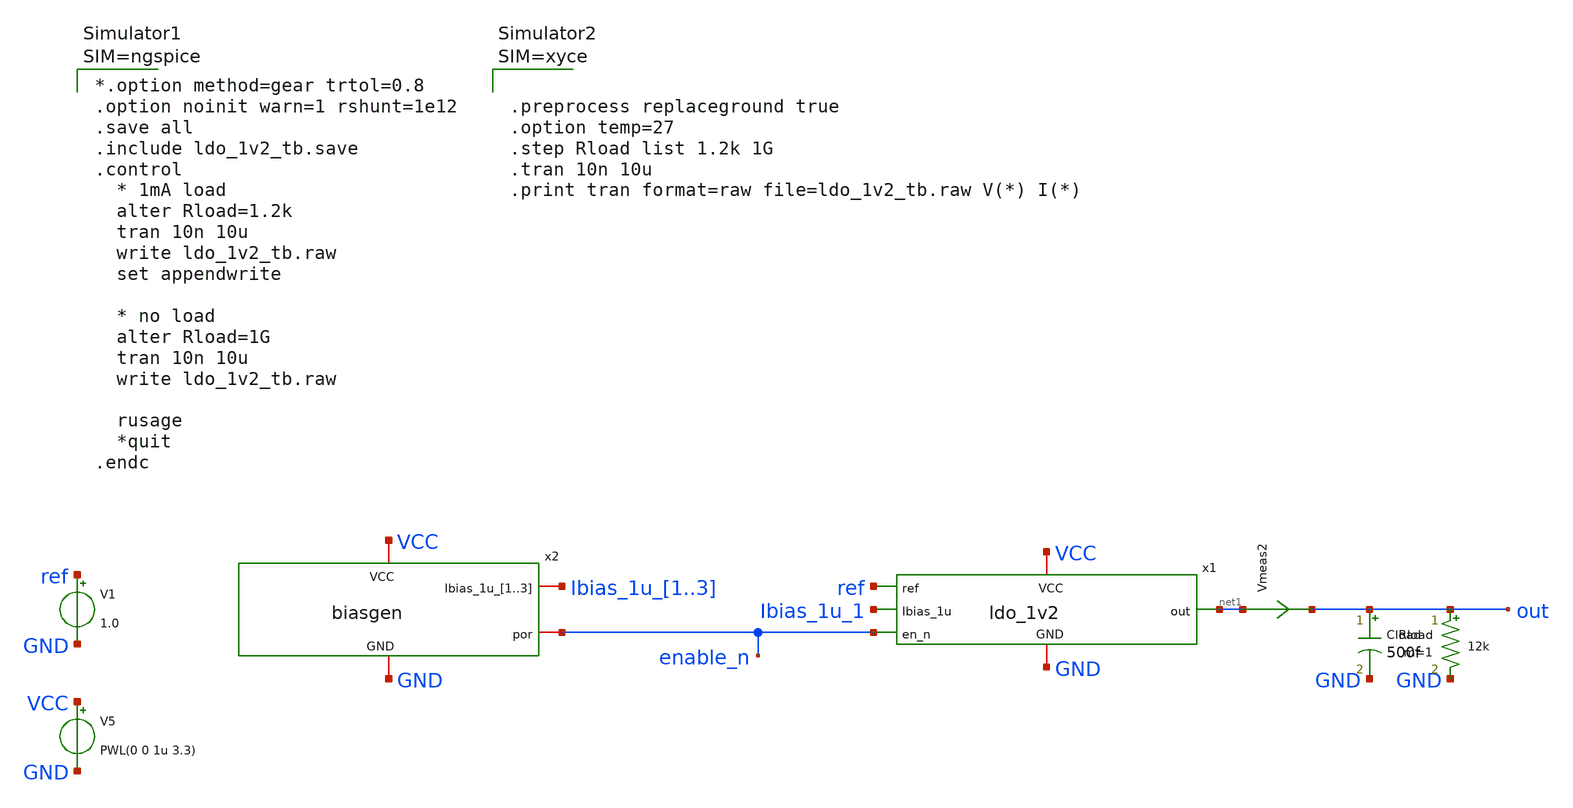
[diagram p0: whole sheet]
** sch_path: FLDO/design_data/xschem/ldo_1v2_tb.sch
**.subckt ldo_1v2_tb
x1 VCC GND ref Ibias_1u_1 net1 enable_n ldo_1v2
x2 VCC GND Ibias_1u_1 Ibias_1u_2 Ibias_1u_3 enable_n biasgen
V5 VCC GND PWL(0 0 1u 3.3)
V1 ref GND 1.0
Cload out GND 500f m=1
Rload out GND 12k m=1
Vmeas2 net1 out 0
.save i(vmeas2)
**** begin user architecture code









** IHP models
.lib cornerMOSlv.lib mos_tt
.lib cornerMOShv.lib mos_tt
.lib cornerHBT.lib hbt_typ
.lib cornerRES.lib res_typ
.lib cornerCAP.lib cap_typ

.include sg13g2_stdcell.spice






*.option method=gear trtol=0.8
.option noinit warn=1 rshunt=1e12
.save all
.include ldo_1v2_tb.save
.control
  * 1mA load
  alter Rload=1.2k
  tran 10n 10u
  write ldo_1v2_tb.raw
  set appendwrite

  * no load
  alter Rload=1G
  tran 10n 10u
  write ldo_1v2_tb.raw

  rusage
  *quit
.endc



**** end user architecture code
**.ends

* expanding   symbol:  ldo_1v2.sym # of pins=6
** sym_path: FLDO/design_data/xschem/ldo_1v2.sym
** sch_path: FLDO/design_data/xschem/ldo_1v2.sch
.subckt ldo_1v2 VCC GND ref Ibias_1u out en_n
*.iopin VCC
*.iopin GND
*.ipin ref
*.ipin Ibias_1u
*.opin out
*.ipin en_n
XM4 out vg net1 net1 sg13_hv_pmos w=50u l=0.4u ng=10 m=1 mm_ok=1
Vmeas VCC net1 0
.save i(vmeas)
XC1 out vg cap_cmim w=10.0e-6 l=10.0e-6 m=1
XM2 Ibias_1u en_n GND GND sg13_hv_nmos w=0.3u l=0.45u ng=1 m=1 mm_ok=1
XM3 vg en VCC VCC sg13_hv_pmos w=0.3u l=0.4u ng=1 m=1 mm_ok=1
XM1 en en_n GND GND sg13_hv_nmos w=0.3u l=0.45u ng=1 m=1 mm_ok=1
XM11 en en_n VCC VCC sg13_hv_pmos w=0.3u l=0.4u ng=1 m=1 mm_ok=1
XRdummy GND GND gnd rhigh w=0.5e-6 l=4e-6 m=2 b=0 mm_ok=1
x1 VCC GND Ibias_1u fb ref vg ldo_ota
XR2 fb out gnd rhigh w=0.5e-6 l=4*4e-6 m=1 b=0
XR1 GND fb gnd rhigh w=0.5e-6 l=20*4e-6 m=1 b=0
.ends


* expanding   symbol:  biasgen.sym # of pins=4
** sym_path: FLDO/design_data/xschem/biasgen.sym
** sch_path: FLDO/design_data/xschem/biasgen.sch
.subckt biasgen VCC GND Ibias_1u_1 Ibias_1u_2 Ibias_1u_3 por
*.iopin VCC
*.iopin GND
*.iopin Ibias_1u_1,Ibias_1u_2,Ibias_1u_3
*.opin por
XM1 vp vn net1 GND sg13_hv_nmos w=2u l=2u ng=1 m=3 mm_ok=1
XM2 vn vn GND GND sg13_hv_nmos w=2u l=2u ng=1 m=1 mm_ok=1
XM3 vn vp VCC VCC sg13_hv_pmos w=0.5u l=2u ng=1 m=2 mm_ok=1
XM4 vp vp VCC VCC sg13_hv_pmos w=0.5u l=2u ng=1 m=2 mm_ok=1
XMout0 Ibias_1u_0 vp VCC VCC sg13_hv_pmos w=0.5u l=2u ng=1 m=1 mm_ok=1
XMout1 Ibias_1u_1 vp VCC VCC sg13_hv_pmos w=0.5u l=2u ng=1 m=1 mm_ok=1
XMout2 Ibias_1u_2 vp VCC VCC sg13_hv_pmos w=0.5u l=2u ng=1 m=1 mm_ok=1
XMout3 Ibias_1u_3 vp VCC VCC sg13_hv_pmos w=0.5u l=2u ng=1 m=1 mm_ok=1
XC1 Ibias_1u_0 GND cap_cmim w=7.0e-6 l=7.0e-6 m=1
XM7 por Ibias_1u_0 VCC VCC sg13_hv_pmos w=0.3u l=0.4u ng=1 m=1 mm_ok=1
XM8 por Ibias_1u_0 GND GND sg13_hv_nmos w=0.3u l=0.45u ng=1 m=1 mm_ok=1
XR1 net1 GND GND rppd w=0.5e-6 l=80e-6 m=1 b=0 mm_ok=1
XM5 vp vstart GND GND sg13_hv_nmos w=0.3u l=0.45u ng=1 m=1 mm_ok=1
XM6 vstart vn GND GND sg13_hv_nmos w=0.3u l=0.45u ng=1 m=1 mm_ok=1
XM9 vstart vn net2 VCC sg13_hv_pmos w=0.3u l=2u ng=1 m=1 mm_ok=1
XM10 net2 net2 net3 VCC sg13_hv_pmos w=0.3u l=2u ng=1 m=1 mm_ok=1
XM11 net3 net3 VCC VCC sg13_hv_pmos w=0.3u l=2u ng=1 m=1 mm_ok=1
.ends


* expanding   symbol:  ldo_ota.sym # of pins=6
** sym_path: FLDO/design_data/xschem/ldo_ota.sym
** sch_path: FLDO/design_data/xschem/ldo_ota.sch
.subckt ldo_ota VCC GND Ibias_1u plus min out
*.iopin VCC
*.iopin GND
*.ipin plus
*.ipin min
*.opin out
*.ipin Ibias_1u
XM5 vbp plus tail GND sg13_hv_nmos w=3u l=2u ng=3 m=1 mm_ok=1
XM6 out min tail GND sg13_hv_nmos w=3u l=2u ng=3 m=1 mm_ok=1
XM7 tail Ibias_1u GND GND sg13_hv_nmos w=1u l=2u ng=1 m=2 mm_ok=1
XM8 Ibias_1u Ibias_1u GND GND sg13_hv_nmos w=1u l=2u ng=1 m=1 mm_ok=1
XM9 out vbp VCC VCC sg13_hv_pmos w=2u l=2u ng=2 m=1 mm_ok=1
XM10 vbp vbp VCC VCC sg13_hv_pmos w=2u l=2u ng=2 m=1 mm_ok=1
XMdummy0 GND Ibias_1u GND GND sg13_hv_nmos w=1u l=2u ng=1 m=2 mm_ok=1
XMdummy1 tail tail tail GND sg13_hv_nmos w=1u l=2u ng=1 m=4 mm_ok=1
XMdummyP VCC vbp VCC VCC sg13_hv_pmos w=1u l=2u ng=1 m=2 mm_ok=1
.ends

.end
